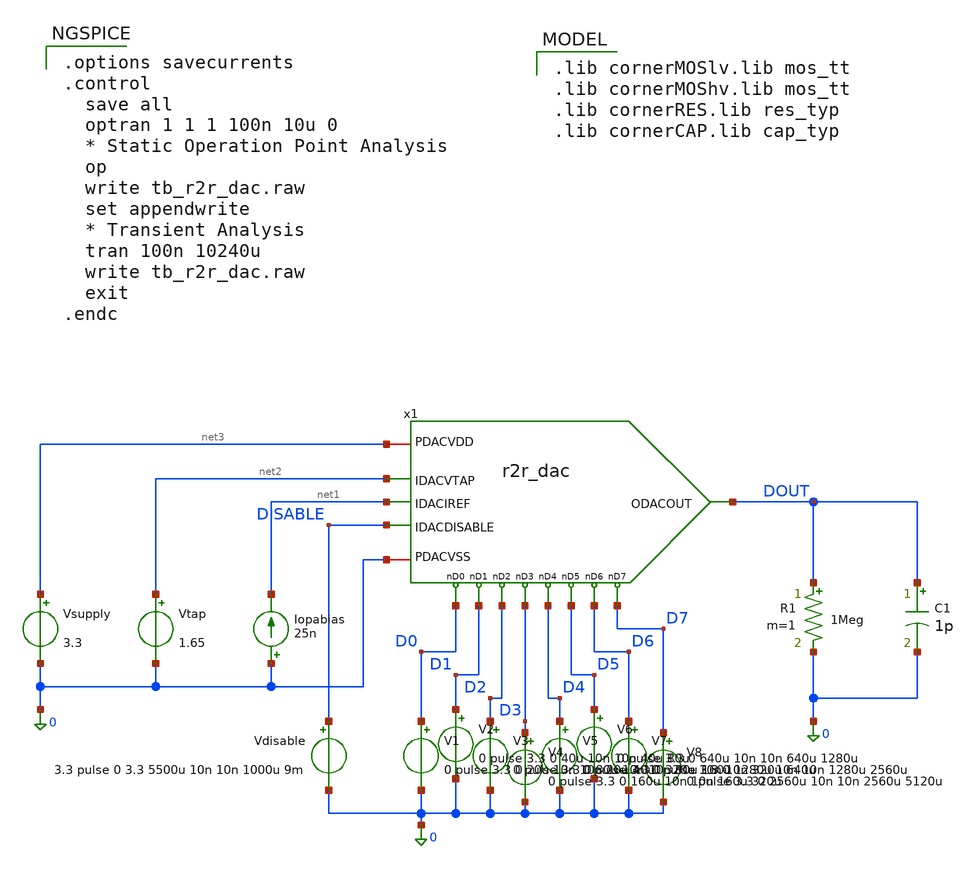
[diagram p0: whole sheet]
** sch_path: macros/heichips26_FAIf/macros/r2r_dac/testbenches/xschem/r2r_dac_tb_tran.sch
**.subckt r2r_dac_tb_tran
x1 net3 DOUT net2 net1 D7 D0 D2 D4 D5 D6 D3 D1 0 DISABLE r2r_dac
Vsupply net3 0 3.3
R1 DOUT 0 1Meg m=1
Vtap net2 0 1.65
Iopabias 0 net1 25n
V1 D0 0 0 pulse 3.3 0 20u 10n 10n 20u 40u
V2 D1 0 0 pulse 3.3 0 40u 10n 10n 40u 80u
V3 D2 0 0 pulse 3.3 0 80u 10n 10n 80u 160u
V4 D3 0 0 pulse 3.3 0 160u 10n 10n 160u 320u
V5 D4 0 0 pulse 3.3 0 320u 10n 10n 320u 640u
V6 D5 0 0 pulse 3.3 0 640u 10n 10n 640u 1280u
V7 D6 0 0 pulse 3.3 0 1280u 10n 10n 1280u 2560u
V8 D7 0 0 pulse 3.3 0 2560u 10n 10n 2560u 5120u
C1 DOUT 0 1p m=1
Vdisable DISABLE 0 3.3 pulse 0 3.3 5500u 10n 10n 1000u 9m
**** begin user architecture code

.options savecurrents
.control
  save all
  optran 1 1 1 100n 10u 0
  * Static Operation Point Analysis
  op
  write tb_r2r_dac.raw
  set appendwrite
  * Transient Analysis
  tran 100n 10240u
  write tb_r2r_dac.raw
  exit
.endc



.lib cornerMOSlv.lib mos_tt
.lib cornerMOShv.lib mos_tt
.lib cornerRES.lib res_typ
.lib cornerCAP.lib cap_typ


**** end user architecture code
**.ends

* expanding   symbol:  r2r_dac.sym # of pins=14
** sym_path: r2r_dac.sym
** sch_path: r2r_dac.sch
.subckt r2r_dac PDACVDD ODACOUT IDACVTAP IDACIREF nD7 nD0 nD2 nD4 nD5 nD6 nD3 nD1 PDACVSS
+ IDACDISABLE
*.iopin PDACVDD
*.iopin PDACVSS
*.ipin nD0
*.ipin nD1
*.ipin nD2
*.ipin IDACIREF
*.opin ODACOUT
*.ipin nD3
*.ipin nD4
*.ipin nD5
*.ipin nD6
*.ipin nD7
*.ipin IDACVTAP
*.ipin IDACDISABLE
XR1 net1 PDACVSS PDACVSS rhigh w=0.5e-6 l=15e-6 m=1 b=0 mm_ok=1
XR2 net8 net1 PDACVSS rhigh w=0.5e-6 l=15e-6 m=1 b=0 mm_ok=1
XR4 net2 nD0 PDACVSS rhigh w=0.5e-6 l=15e-6 m=1 b=0 mm_ok=1
XR5 net7 net2 PDACVSS rhigh w=0.5e-6 l=15e-6 m=1 b=0 mm_ok=1
XR6 net3 nD1 PDACVSS rhigh w=0.5e-6 l=15e-6 m=1 b=0 mm_ok=1
XR7 net6 net3 PDACVSS rhigh w=0.5e-6 l=15e-6 m=1 b=0 mm_ok=1
XR8 net4 nD2 PDACVSS rhigh w=0.5e-6 l=15e-6 m=1 b=0 mm_ok=1
XR9 net5 net4 PDACVSS rhigh w=0.5e-6 l=15e-6 m=1 b=0 mm_ok=1
XR10 net7 net8 PDACVSS rhigh w=0.5e-6 l=15e-6 m=1 b=0 mm_ok=1
XR11 net6 net7 PDACVSS rhigh w=0.5e-6 l=15e-6 m=1 b=0 mm_ok=1
XR12 net5 net6 PDACVSS rhigh w=0.5e-6 l=15e-6 m=1 b=0 mm_ok=1
XR14 UNBUF_DAC net9 PDACVSS rhigh w=0.5e-6 l=14e-6 m=1 b=0 mm_ok=1
XR3 net10 nD3 PDACVSS rhigh w=0.5e-6 l=15e-6 m=1 b=0 mm_ok=1
XR13 net13 net10 PDACVSS rhigh w=0.5e-6 l=15e-6 m=1 b=0 mm_ok=1
XR15 net11 nD4 PDACVSS rhigh w=0.5e-6 l=15e-6 m=1 b=0 mm_ok=1
XR16 net12 net11 PDACVSS rhigh w=0.5e-6 l=15e-6 m=1 b=0 mm_ok=1
XR17 net13 net5 PDACVSS rhigh w=0.5e-6 l=15e-6 m=1 b=0 mm_ok=1
XR18 net12 net13 PDACVSS rhigh w=0.5e-6 l=15e-6 m=1 b=0 mm_ok=1
XR19 net14 nD5 PDACVSS rhigh w=0.5e-6 l=15e-6 m=1 b=0 mm_ok=1
XR20 net17 net14 PDACVSS rhigh w=0.5e-6 l=15e-6 m=1 b=0 mm_ok=1
XR21 net15 nD6 PDACVSS rhigh w=0.5e-6 l=15e-6 m=1 b=0 mm_ok=1
XR22 net16 net15 PDACVSS rhigh w=0.5e-6 l=15e-6 m=1 b=0 mm_ok=1
XR23 net17 net12 PDACVSS rhigh w=0.5e-6 l=15e-6 m=1 b=0 mm_ok=1
XR24 net16 net17 PDACVSS rhigh w=0.5e-6 l=15e-6 m=1 b=0 mm_ok=1
XR25 net18 nD7 PDACVSS rhigh w=0.5e-6 l=15e-6 m=1 b=0 mm_ok=1
XR26 UNBUF_DAC net18 PDACVSS rhigh w=0.5e-6 l=15e-6 m=1 b=0 mm_ok=1
XR27 UNBUF_DAC net16 PDACVSS rhigh w=0.5e-6 l=15e-6 m=1 b=0 mm_ok=1
x1 PDACVDD IDACIREF UNBUF_DAC ODACOUT IDACVTAP PDACVSS IDACDISABLE op_amp_ver_2
XM1 net9 nIDACDISABLE ODACOUT PDACVSS sg13_hv_nmos w=1u l=0.45u ng=1 m=1 mm_ok=1
XM2 ODACOUT IDACDISABLE net9 PDACVDD sg13_hv_pmos w=2u l=0.45u ng=1 m=1 mm_ok=1
XRD2 PDACVSS PDACVSS PDACVSS rhigh w=0.5e-6 l=15e-6 m=1 b=0 mm_ok=1
XRD1 PDACVSS PDACVSS PDACVSS rhigh w=0.5e-6 l=15e-6 m=1 b=0 mm_ok=1
XRD3 PDACVSS PDACVSS PDACVSS rhigh w=0.5e-6 l=14e-6 m=1 b=0 mm_ok=1
XM3 nIDACDISABLE IDACDISABLE PDACVSS PDACVSS sg13_hv_nmos w=0.3u l=0.45u ng=1 m=1 mm_ok=1
XM4 nIDACDISABLE IDACDISABLE PDACVDD PDACVDD sg13_hv_pmos w=0.6u l=0.45u ng=1 m=1 mm_ok=1
.ends


* expanding   symbol:  ../../../opamp/schematic/xschem/op_amp_ver_2.sym # of pins=7
** sym_path: ../../../opamp/schematic/xschem/op_amp_ver_2.sym
** sch_path: ../../../opamp/schematic/xschem/op_amp_ver_2.sch
.subckt op_amp_ver_2 POAVDD IOAIREF IOAM OOA IOAP POAVSS IOADISABLE
*.iopin POAVDD
*.ipin IOAM
*.ipin IOAP
*.opin OOA
*.ipin IOAIREF
*.iopin POAVSS
*.ipin IOADISABLE
XMP13 net1 net1 POAVDD POAVDD sg13_hv_pmos w=2.4u l=0.4u ng=1 m=1 mm_ok=1
XMP14 ptlg ptlg net1 POAVDD sg13_hv_pmos w=2.4u l=0.4u ng=1 m=1 mm_ok=1
XMN16 ptlg ncasc net2 POAVSS sg13_hv_nmos w=0.6u l=0.6u ng=1 m=1 mm_ok=1
XMN13 net2 nbias POAVSS POAVSS sg13_hv_nmos w=0.6u l=2.4u ng=1 m=1 mm_ok=1
XMN18 ntlg ntlg net3 POAVSS sg13_hv_nmos w=1.2u l=0.6u ng=1 m=1 mm_ok=1
XMN17 net3 net3 POAVSS POAVSS sg13_hv_nmos w=1.2u l=0.6u ng=1 m=1 mm_ok=1
XMP10 net11 pbias POAVDD POAVDD sg13_hv_pmos w=1.2u l=1.2u ng=1 m=1 mm_ok=1
XMP12 ntlg pcasc net11 POAVDD sg13_hv_pmos w=1.2u l=0.6u ng=1 m=1 mm_ok=1
XMP1 net9 pbias POAVDD POAVDD sg13_hv_pmos w=1.2u l=1.2u ng=1 m=4 mm_ok=1
XMP2 net10 pbias POAVDD POAVDD sg13_hv_pmos w=1.2u l=1.2u ng=1 m=4 mm_ok=1
XMN1 net9 IOAM net5 POAVSS sg13_hv_nmos w=4.8u l=0.45u ng=1 m=1 mm_ok=1
XMN2 net10 IOAP net5 POAVSS sg13_hv_nmos w=4.8u l=0.45u ng=1 m=1 mm_ok=1
XMN3 net4 nbias POAVSS POAVSS sg13_hv_nmos w=0.6u l=2.4u ng=1 m=8 mm_ok=1
XMN6 net5 ncasc net4 POAVSS sg13_hv_nmos w=0.6u l=0.6u ng=1 m=8 mm_ok=1
XMN7 net8 ncasc net7 POAVSS sg13_hv_nmos w=0.6u l=0.6u ng=1 m=8 mm_ok=1
XMN8 ndrive ncasc net6 POAVSS sg13_hv_nmos w=0.6u l=0.6u ng=1 m=8 mm_ok=1
XMN4 net7 net8 POAVSS POAVSS sg13_hv_nmos w=0.6u l=2.4u ng=1 m=8 mm_ok=1
XMN5 net6 net8 POAVSS POAVSS sg13_hv_nmos w=0.6u l=2.4u ng=1 m=8 mm_ok=1
XMP3 net9 pbias POAVDD POAVDD sg13_hv_pmos w=1.2u l=1.2u ng=1 m=4 mm_ok=1
XMP5 net8 pcasc net9 POAVDD sg13_hv_pmos w=1.2u l=0.6u ng=1 m=8 mm_ok=1
XMP4 net10 pbias POAVDD POAVDD sg13_hv_pmos w=1.2u l=1.2u ng=1 m=4 mm_ok=1
XMP6 pdrive pcasc net10 POAVDD sg13_hv_pmos w=1.2u l=0.6u ng=1 m=8 mm_ok=1
XMP7 ndrive ptlg pdrive POAVDD sg13_hv_pmos w=2.4u l=0.4u ng=1 m=4 mm_ok=1
XMN9 pdrive ntlg ndrive POAVSS sg13_hv_nmos w=1.2u l=0.6u ng=1 m=4 mm_ok=1
XMP8 OOA pdrive POAVDD POAVDD sg13_hv_pmos w=2.4u l=0.4u ng=1 m=40 mm_ok=1
XMN10 OOA ndrive POAVSS POAVSS sg13_hv_nmos w=1.2u l=0.6u ng=1 m=40 mm_ok=1
XMN20 IOAIREF IOAIREF POAVSS POAVSS sg13_hv_nmos w=0.6u l=2.4u ng=1 m=1 mm_ok=1
XMN21 pcasc IOAIREF POAVSS POAVSS sg13_hv_nmos w=0.6u l=2.4u ng=1 m=1 mm_ok=1
XMN22 pbias IOAIREF POAVSS POAVSS sg13_hv_nmos w=0.6u l=2.4u ng=1 m=1 mm_ok=1
XMN23 net19 ncasc POAVSS POAVSS sg13_hv_nmos w=0.4u l=10u ng=1 m=1 mm_ok=1
XMN25 net13 nbias POAVSS POAVSS sg13_hv_nmos w=0.6u l=2.4u ng=1 m=1 mm_ok=1
XMN24 ncasc ncasc net22 POAVSS sg13_hv_nmos w=0.4u l=10u ng=1 m=1 mm_ok=1
XMN26 nbias ncasc net13 POAVSS sg13_hv_nmos w=0.6u l=0.6u ng=1 m=1 mm_ok=1
XMP21 pcasc pcasc net18 POAVDD sg13_hv_pmos w=1u l=10u ng=1 m=1 mm_ok=1
XMP20 net18 pcasc net17 POAVDD sg13_hv_pmos w=1u l=10.0u ng=1 m=1 mm_ok=1
XMP22 net12 pbias POAVDD POAVDD sg13_hv_pmos w=1.2u l=1.2u ng=1 m=1 mm_ok=1
XMP25 pbias pcasc net12 POAVDD sg13_hv_pmos w=1.2u l=0.6u ng=1 m=1 mm_ok=1
XMP26 ncasc pcasc net15 POAVDD sg13_hv_pmos w=1.2u l=0.6u ng=1 m=1 mm_ok=1
XMP23 net15 pbias POAVDD POAVDD sg13_hv_pmos w=1.2u l=1.2u ng=1 m=1 mm_ok=1
XMP24 net14 pbias POAVDD POAVDD sg13_hv_pmos w=1.2u l=1.2u ng=1 m=1 mm_ok=1
XMP27 nbias pcasc net14 POAVDD sg13_hv_pmos w=1.2u l=0.6u ng=1 m=1 mm_ok=1
XMP16 net17 pcasc net16 POAVDD sg13_hv_pmos w=1u l=10.0u ng=1 m=1 mm_ok=1
XMN11 net20 ncasc net19 POAVSS sg13_hv_nmos w=0.4u l=10u ng=1 m=1 mm_ok=1
XMP28 net16 pcasc POAVDD POAVDD sg13_hv_pmos w=1u l=10.0u ng=1 m=1 mm_ok=1
XMN12 net21 ncasc net20 POAVSS sg13_hv_nmos w=0.4u l=10u ng=1 m=1 mm_ok=1
XMN14 net22 ncasc net21 POAVSS sg13_hv_nmos w=0.4u l=10u ng=1 m=1 mm_ok=1
XMDP1 POAVDD pbias POAVDD POAVDD sg13_hv_pmos w=1.2u l=1.2u ng=1 m=1 mm_ok=1
XMDP2 POAVDD pbias POAVDD POAVDD sg13_hv_pmos w=1.2u l=1.2u ng=1 m=1 mm_ok=1
XMDOP1 POAVDD pcasc POAVDD POAVDD sg13_hv_pmos w=1.2u l=0.6u ng=1 m=1 mm_ok=1
XMDOP2 POAVDD pcasc POAVDD POAVDD sg13_hv_pmos w=1.2u l=0.6u ng=1 m=1 mm_ok=1
XMDOP3 POAVDD pcasc POAVDD POAVDD sg13_hv_pmos w=1.2u l=0.6u ng=1 m=1 mm_ok=1
XMDOP4 POAVDD pcasc POAVDD POAVDD sg13_hv_pmos w=1.2u l=0.6u ng=1 m=1 mm_ok=1
XMDN1 POAVSS nbias POAVSS POAVSS sg13_hv_nmos w=0.6u l=2.4u ng=1 m=1 mm_ok=1
XMDN2 POAVSS nbias POAVSS POAVSS sg13_hv_nmos w=0.6u l=2.4u ng=1 m=1 mm_ok=1
XMDON1 nIOADISABLE IOADISABLE POAVSS POAVSS sg13_hv_nmos w=0.6u l=0.6u ng=1 m=1 mm_ok=1
XMDON2 ntlg IOADISABLE POAVSS POAVSS sg13_hv_nmos w=0.6u l=0.6u ng=1 m=1 mm_ok=1
XMDON3 ndrive IOADISABLE POAVSS POAVSS sg13_hv_nmos w=0.6u l=0.6u ng=1 m=1 mm_ok=1
XMDON4 IOAIREF IOADISABLE POAVSS POAVSS sg13_hv_nmos w=0.6u l=0.6u ng=1 m=1 mm_ok=1
XMDP7 POAVDD pbias POAVDD POAVDD sg13_hv_pmos w=1.2u l=1.2u ng=1 m=1 mm_ok=1
XMDP8 POAVDD pbias POAVDD POAVDD sg13_hv_pmos w=1.2u l=1.2u ng=1 m=1 mm_ok=1
XMDN7 POAVSS nbias POAVSS POAVSS sg13_hv_nmos w=0.6u l=2.4u ng=1 m=1 mm_ok=1
XMDN8 POAVSS nbias POAVSS POAVSS sg13_hv_nmos w=0.6u l=2.4u ng=1 m=1 mm_ok=1
XMDN9 POAVSS POAVSS POAVSS POAVSS sg13_hv_nmos w=1.2u l=0.45u ng=1 m=1 mm_ok=1
XMDN10 POAVSS POAVSS POAVSS POAVSS sg13_hv_nmos w=1.2u l=0.45u ng=1 m=1 mm_ok=1
XMDN11 POAVSS POAVSS POAVSS POAVSS sg13_hv_nmos w=1.2u l=0.45u ng=1 m=1 mm_ok=1
XMDN12 POAVSS POAVSS POAVSS POAVSS sg13_hv_nmos w=1.2u l=0.45u ng=1 m=1 mm_ok=1
XMDN13 POAVSS POAVSS POAVSS POAVSS sg13_hv_nmos w=2.4u l=0.45u ng=1 m=1 mm_ok=1
XMDN14 POAVSS POAVSS POAVSS POAVSS sg13_hv_nmos w=2.4u l=0.45u ng=1 m=1 mm_ok=1
XMDN15 POAVSS POAVSS POAVSS POAVSS sg13_hv_nmos w=2.4u l=0.45u ng=1 m=1 mm_ok=1
XMDN16 POAVSS POAVSS POAVSS POAVSS sg13_hv_nmos w=2.4u l=0.45u ng=1 m=1 mm_ok=1
XMDN17 POAVSS POAVSS POAVSS POAVSS sg13_hv_nmos w=1.2u l=0.45u ng=1 m=1 mm_ok=1
XMDN18 POAVSS POAVSS POAVSS POAVSS sg13_hv_nmos w=1.2u l=0.45u ng=1 m=1 mm_ok=1
XMDN19 POAVSS POAVSS POAVSS POAVSS sg13_hv_nmos w=1.2u l=0.45u ng=1 m=1 mm_ok=1
XMDN20 POAVSS POAVSS POAVSS POAVSS sg13_hv_nmos w=1.2u l=0.45u ng=1 m=1 mm_ok=1
XMDN21 POAVSS IOAIREF POAVSS POAVSS sg13_hv_nmos w=0.6u l=2.4u ng=1 m=1 mm_ok=1
XMDN22 POAVSS IOAIREF POAVSS POAVSS sg13_hv_nmos w=0.6u l=2.4u ng=1 m=1 mm_ok=1
XMDP9 POAVDD pcasc POAVDD POAVDD sg13_hv_pmos w=1u l=10u ng=1 m=1 mm_ok=1
XMDN23 POAVSS ncasc POAVSS POAVSS sg13_hv_nmos w=0.4u l=10u ng=1 m=1 mm_ok=1
XMDP10 POAVDD pcasc POAVDD POAVDD sg13_hv_pmos w=1u l=10u ng=1 m=1 mm_ok=1
XMDN24 POAVSS ncasc POAVSS POAVSS sg13_hv_nmos w=0.4u l=10u ng=1 m=1 mm_ok=1
XMDP11 POAVDD pbias POAVDD POAVDD sg13_hv_pmos w=1.2u l=1.2u ng=1 m=1 mm_ok=1
XMDP12 POAVDD pbias POAVDD POAVDD sg13_hv_pmos w=1.2u l=1.2u ng=1 m=1 mm_ok=1
XMDP13 POAVDD pcasc POAVDD POAVDD sg13_hv_pmos w=1.2u l=0.6u ng=1 m=1 mm_ok=1
XMDP14 POAVDD pcasc POAVDD POAVDD sg13_hv_pmos w=1.2u l=0.6u ng=1 m=1 mm_ok=1
XMDN25 POAVSS POAVSS POAVSS POAVSS sg13_hv_nmos w=0.6u l=2.4u ng=1 m=1 mm_ok=1
XMDN26 POAVSS POAVSS POAVSS POAVSS sg13_hv_nmos w=0.6u l=2.4u ng=1 m=1 mm_ok=1
XMDN27 POAVSS ncasc POAVSS POAVSS sg13_hv_nmos w=0.6u l=0.6u ng=1 m=1 mm_ok=1
XMDN28 POAVSS ncasc POAVSS POAVSS sg13_hv_nmos w=0.6u l=0.6u ng=1 m=1 mm_ok=1
XMDP15 POAVDD POAVDD POAVDD POAVDD sg13_hv_pmos w=2.4u l=0.4u ng=1 m=8 mm_ok=1
XMDN29 POAVSS POAVSS POAVSS POAVSS sg13_hv_nmos w=1.2u l=0.6u ng=1 m=8 mm_ok=1
XMDP16 POAVDD POAVDD POAVDD POAVDD sg13_hv_pmos w=2.4u l=0.4u ng=1 m=2 mm_ok=1
XMDN30 POAVSS POAVSS POAVSS POAVSS sg13_hv_nmos w=1.2u l=0.6u ng=1 m=2 mm_ok=1
XMDP17 POAVDD POAVDD POAVDD POAVDD sg13_hv_pmos w=2.4u l=0.4u ng=1 m=8 mm_ok=1
XMDN31 POAVSS POAVSS POAVSS POAVSS sg13_hv_nmos w=1.2u l=0.6u ng=1 m=8 mm_ok=1
XMDOP5 nIOADISABLE IOADISABLE POAVDD POAVDD sg13_hv_pmos w=1.2u l=0.6u ng=1 m=1 mm_ok=1
XMDOP6 ptlg nIOADISABLE POAVDD POAVDD sg13_hv_pmos w=1.2u l=0.6u ng=1 m=1 mm_ok=1
XMDOP7 pdrive nIOADISABLE POAVDD POAVDD sg13_hv_pmos w=1.2u l=0.6u ng=1 m=1 mm_ok=1
XMDOP8 pcasc nIOADISABLE POAVDD POAVDD sg13_hv_pmos w=1.2u l=0.6u ng=1 m=1 mm_ok=1
XC1 pdrive OOA cap_cmomi w=40e-6 l=14e-6 mmin=1 mmax=3 feed=double subblock=0 m=1 mm_ok=1
XC2 ndrive OOA cap_cmomi w=40e-6 l=14e-6 mmin=1 mmax=3 feed=double subblock=0 m=1 mm_ok=1
.ends

.end
